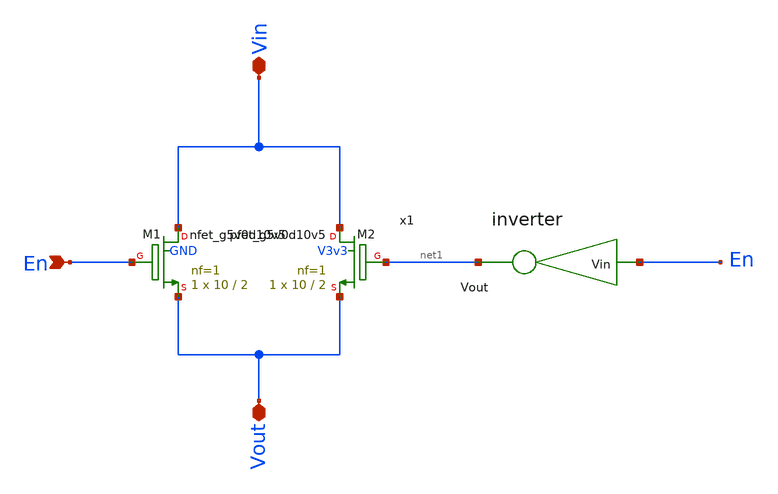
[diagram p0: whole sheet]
** sch_path: xschem/StandardCells/TransmissionGate.sch
**.subckt TransmissionGate Vout Vin En
*.iopin Vout
*.iopin Vin
*.ipin En
XM1 Vin En Vout GND sky130_fd_pr__nfet_g5v0d10v5 L=2 W=10 nf=1 ad='int((nf+1)/2) * W/nf * 0.29' as='int((nf+2)/2) * W/nf * 0.29'
+ pd='2*int((nf+1)/2) * (W/nf + 0.29)' ps='2*int((nf+2)/2) * (W/nf + 0.29)' nrd='0.29 / W' nrs='0.29 / W'
+ sa=0 sb=0 sd=0 mult=1 m=1
XM2 Vin net1 Vout V3v3 sky130_fd_pr__pfet_g5v0d10v5 L=2 W=10 nf=1 ad='int((nf+1)/2) * W/nf * 0.29' as='int((nf+2)/2) * W/nf * 0.29'
+ pd='2*int((nf+1)/2) * (W/nf + 0.29)' ps='2*int((nf+2)/2) * (W/nf + 0.29)' nrd='0.29 / W' nrs='0.29 / W'
+ sa=0 sb=0 sd=0 mult=1 m=1
x1 net1 En inverter
**.ends
.end
